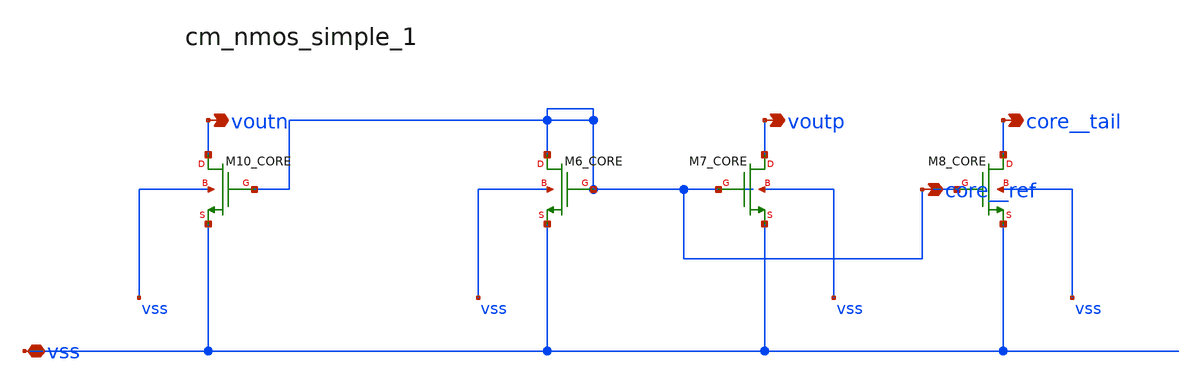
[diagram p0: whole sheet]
** sch_path: analog-db/raw/amp_030_miller_cmfb_composite/hier/blocks/cm_nmos_simple_1.sch
**.subckt cm_nmos_simple_1 vss voutn core__ref voutp core__tail
*.iopin vss
*.opin voutn
*.opin core__ref
*.opin voutp
*.opin core__tail
XM10_CORE voutn core__ref vss vss sg13_lv_nmos w=x_dut_xm10_core_w l=x_dut_xm10_core_l ng=1
+ m=x_dut_xm10_core_m
XM6_CORE core__ref core__ref vss vss sg13_lv_nmos w=x_dut_xm6_core_w l=x_dut_xm6_core_l ng=1
+ m=x_dut_xm6_core_m
XM7_CORE voutp core__ref vss vss sg13_lv_nmos w=x_dut_xm7_core_w l=x_dut_xm7_core_l ng=1
+ m=x_dut_xm7_core_m
XM8_CORE core__tail core__ref vss vss sg13_lv_nmos w=x_dut_xm8_core_w l=x_dut_xm8_core_l ng=1
+ m=x_dut_xm8_core_m
**.ends
.end
